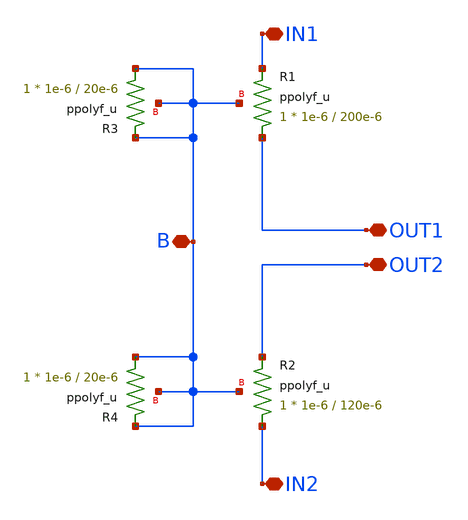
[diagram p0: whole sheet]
** sch_path: LDO/xschem/resistor/symbol/resistor.sch
**.subckt resistor OUT1 IN2 IN1 B OUT2
*.iopin OUT1
*.iopin IN2
*.iopin IN1
*.iopin B
*.iopin OUT2
XR1 OUT1 IN1 B ppolyf_u r_width=1e-6 r_length=200e-6 m=1
XR2 IN2 OUT2 B ppolyf_u r_width=1e-6 r_length=120e-6 m=1
XR3 B B B ppolyf_u r_width=1e-6 r_length=20e-6 m=1
XR4 B B B ppolyf_u r_width=1e-6 r_length=20e-6 m=1
**.ends
.end
